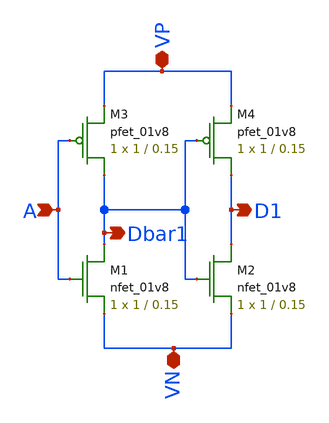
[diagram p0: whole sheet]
** sch_path: mp2/xschem/shiftregister/shift_register_inverter_2.sch
**.subckt shift_register_inverter_2 VP VN A D1 Dbar1
*.iopin VP
*.iopin VN
*.ipin A
*.opin D1
*.opin Dbar1
XM1 Dbar1 A VN GND sky130_fd_pr__nfet_01v8 L=0.15 W=1 nf=1 ad='int((nf+1)/2) * W/nf * 0.29' as='int((nf+2)/2) * W/nf * 0.29'
+ pd='2*int((nf+1)/2) * (W/nf + 0.29)' ps='2*int((nf+2)/2) * (W/nf + 0.29)' nrd='0.29 / W' nrs='0.29 / W'
+ sa=0 sb=0 sd=0 mult=1 m=1
XM2 D1 Dbar1 VN GND sky130_fd_pr__nfet_01v8 L=0.15 W=1 nf=1 ad='int((nf+1)/2) * W/nf * 0.29' as='int((nf+2)/2) * W/nf * 0.29'
+ pd='2*int((nf+1)/2) * (W/nf + 0.29)' ps='2*int((nf+2)/2) * (W/nf + 0.29)' nrd='0.29 / W' nrs='0.29 / W'
+ sa=0 sb=0 sd=0 mult=1 m=1
XM3 Dbar1 A VP VDD sky130_fd_pr__pfet_01v8 L=0.15 W=1 nf=1 ad='int((nf+1)/2) * W/nf * 0.29' as='int((nf+2)/2) * W/nf * 0.29'
+ pd='2*int((nf+1)/2) * (W/nf + 0.29)' ps='2*int((nf+2)/2) * (W/nf + 0.29)' nrd='0.29 / W' nrs='0.29 / W'
+ sa=0 sb=0 sd=0 mult=1 m=1
XM4 D1 Dbar1 VP VDD sky130_fd_pr__pfet_01v8 L=0.15 W=1 nf=1 ad='int((nf+1)/2) * W/nf * 0.29' as='int((nf+2)/2) * W/nf * 0.29'
+ pd='2*int((nf+1)/2) * (W/nf + 0.29)' ps='2*int((nf+2)/2) * (W/nf + 0.29)' nrd='0.29 / W' nrs='0.29 / W'
+ sa=0 sb=0 sd=0 mult=1 m=1
**.ends
.end
